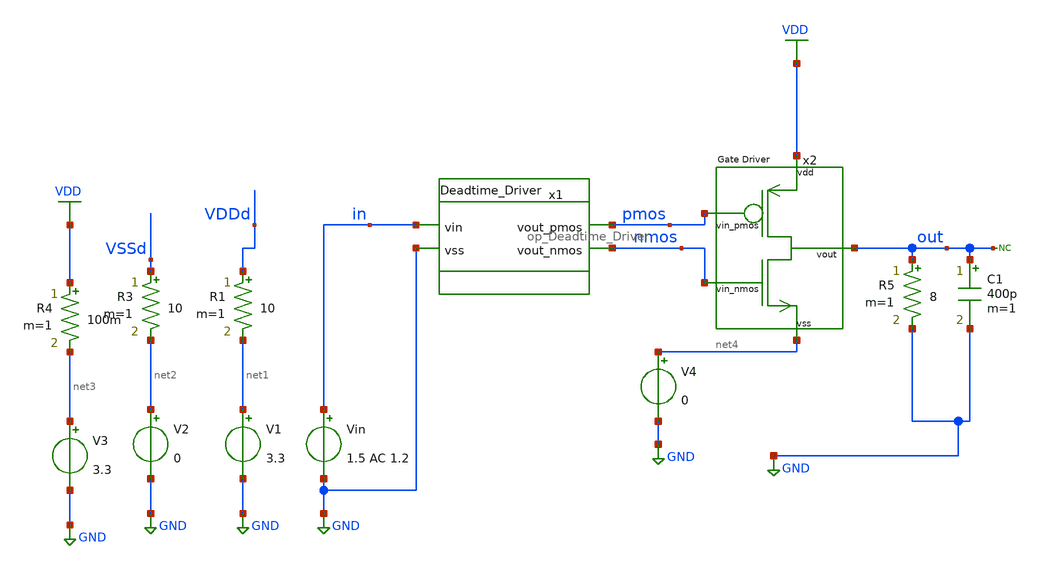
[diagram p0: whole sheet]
** sch_path: designs/libs/tb_analog_pads_pex/tb_op_Deadtime_Driver/tb_temp_deadtime_driver.sch
**.subckt tb_temp_deadtime_driver
V1 net1 GND 3.3
Vin in GND 1.5 AC 1.2
R1 VDDd net1 10 m=1
V2 net2 GND 0
R3 VSSd net2 10 m=1
x1 pmos in nmos GND op_Deadtime_Driver
* noconn out
V3 net3 GND 3.3
R4 VDD net3 100m m=1
R5 out GND 8 m=1
C1 out GND 400p m=1
x2 VDD pmos out nmos net4 Output_Stage
V4 net4 GND 0
**** begin user architecture code

.include $::180MCU_MODELS/design.ngspice
.include /foss/pdks/gf180mcuD/libs.ref/gf180mcu_fd_sc_mcu9t5v0/spice/gf180mcu_fd_sc_mcu9t5v0.spice
.lib $::180MCU_MODELS/sm141064.ngspice typical
.lib $::180MCU_MODELS/sm141064.ngspice cap_mim
.lib $::180MCU_MODELS/sm141064.ngspice mimcap_typical



.temp 27
.options savecurrents
.global VDDd VSSd
.control
save all
**Frequency & time settings
let fsig = 200k
let tper=1/fsig
let tfr = 0.01*tper
let ton = 0.5*tper-2*tfr

let tstop = 4 * tper
let tstep = 0.001*tper


**voltages
alter @Vin[PULSE] = [ 0 2.3 0 $&tfr $&tfr $&ton $&tper 3 ]
alter @Vin[DC] = 3.3
*alter @Vin[SIN] = [ 1.7 1.5 $&fsig 0 0 ]

**simulation
OP
*show all > op.log
show all

**Temperature analysis
tran $&tstep $&tstop
let t = $temp
print t
*plot nmos pmos
plot out
meas tran tfall_p WHEN v(pmos)=0.68 FALL=3
meas tran tfall_n WHEN v(nmos)=0.68 FALL=3

meas tran trise_p WHEN v(pmos)=0.68 RISE=3
meas tran trise_n WHEN v(nmos)=0.68 RISE=3

let delay_fall = $&tfall_p - $&tfall_n
let delay_rise = $&trise_p - $&trise_n

print delay_fall
print delay_rise

**check shoot-through
plot @r5[i] v3#branch v4#branch

*@m.xm1.m0[id]
*plot @m.xm1.m0[id]

plot v4#branch

meas tran v_max MAX v(out)
meas tran v_min MIN v(out)
let vpp = $&v_max - $&v_min
print vpp
write Deadtime_Driver_temp_tb.txt
.endc


**** end user architecture code
**.ends
.GLOBAL GND
.GLOBAL VDD
.end
